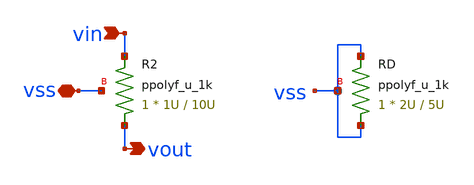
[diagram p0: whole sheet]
** sch_path: LDO/xschem/ota_res/symbol/ota_res.sch
**.subckt ota_res vin vss vout
*.ipin vin
*.iopin vss
*.opin vout
XR2 vout vin vss ppolyf_u_1k r_width=1U r_length=10U m=1
XRD vss vss vss ppolyf_u_1k r_width=2U r_length=5U m=1
**.ends
.end
